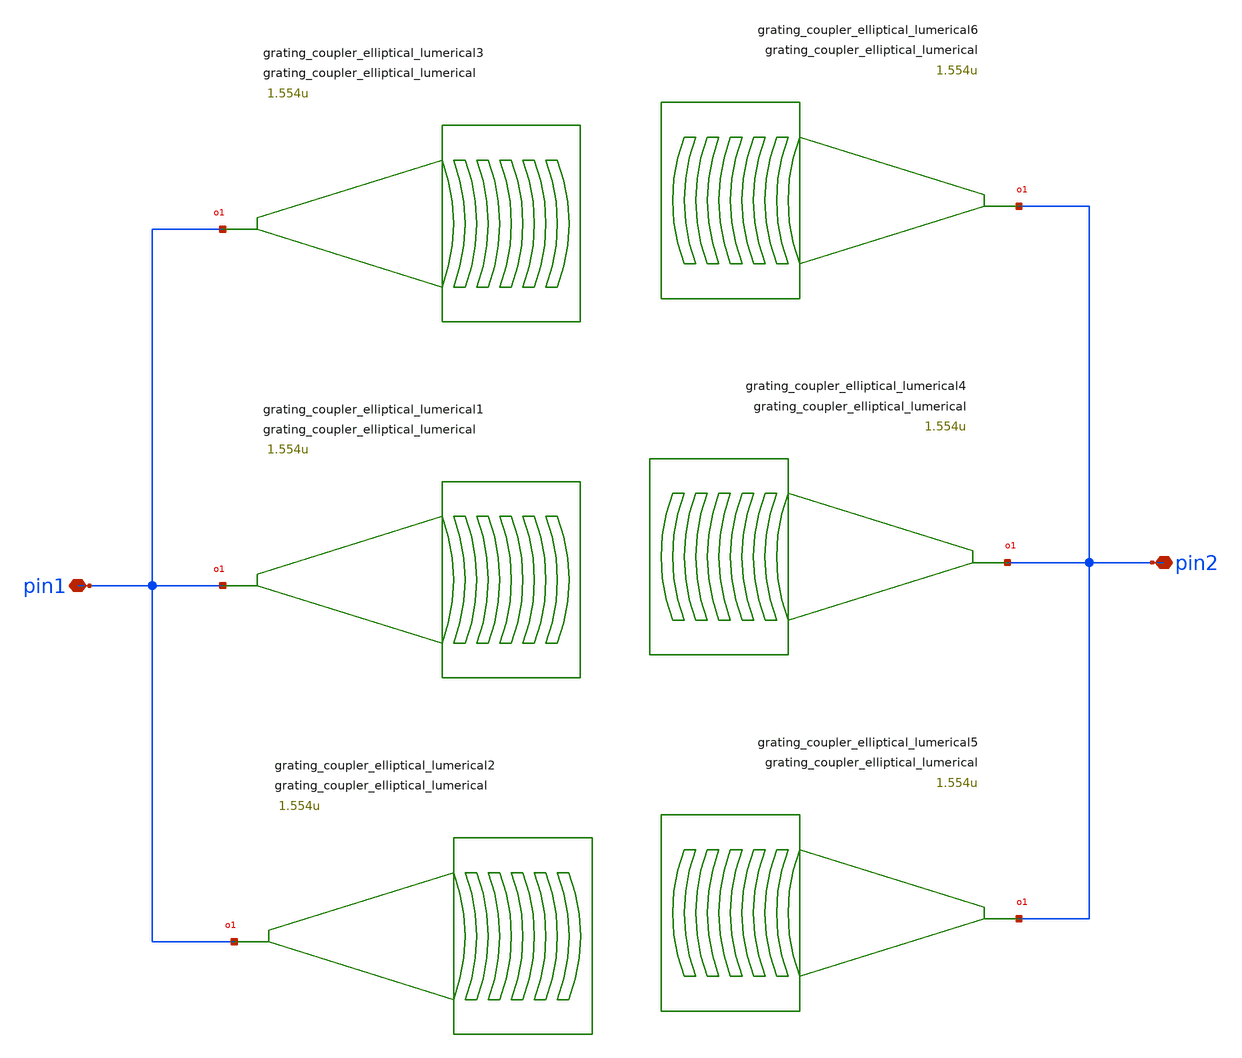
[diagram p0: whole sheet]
** sch_path: xschem/tests/test_sch/test_grating_coupler_elliptical_lumerical.sch
* Copyright (c) 2024, Mabrains LLC
* Licensed under the GNU Lesser General Public License, Version 3.0 (the "License");
* you may not use this file except in compliance with the License.
* GNU Lesser General Public License
* Version 3, 29 June 2007
* This program is free software: you can redistribute it and/or modify
* it under the terms of the GNU Lesser General Public License as published
* by the Free Software Foundation, either version 3 of the License, or
* (at your option) any later version.
* This program is distributed in the hope that it will be useful,
* but WITHOUT ANY WARRANTY; without even the implied warranty of
* MERCHANTABILITY or FITNESS FOR A PARTICULAR PURPOSE.  See the
* GNU Lesser General Public License for more details.
* You should have received a copy of the GNU Lesser General Public License
* along with this program.  If not, see <https://www.gnu.org/licenses/>.
* SPDX-License-Identifier: LGPL-3.0
**.subckt test_grating_coupler_elliptical_lumerical pin1 pin2
*.iopin pin1
*.iopin pin2
Pgrating_coupler_elliptical_lumerical1 pin1 grating_coupler_elliptical_lumerical parameters=[-2.43u,
+ 0.1u, 0.48u] taper_angle=55.0 taper_length=12.6u fiber_angle=5.0 bias_gap=0.0u wavelength=1.554u
Pgrating_coupler_elliptical_lumerical2 pin1 grating_coupler_elliptical_lumerical parameters=[-2.43u,
+ 0.1u, 0.48u] taper_angle=55.0 taper_length=12.6u fiber_angle=5.0 bias_gap=0.0u wavelength=1.554u
Pgrating_coupler_elliptical_lumerical3 pin1 grating_coupler_elliptical_lumerical parameters=[-2.43u,
+ 0.1u, 0.48u] taper_angle=55.0 taper_length=12.6u fiber_angle=5.0 bias_gap=0.0u wavelength=1.554u
Pgrating_coupler_elliptical_lumerical4 pin2 grating_coupler_elliptical_lumerical parameters=[-2.43u,
+ 0.1u, 0.48u] taper_angle=55.0 taper_length=12.6u fiber_angle=5.0 bias_gap=0.0u wavelength=1.554u
Pgrating_coupler_elliptical_lumerical5 pin2 grating_coupler_elliptical_lumerical parameters=[-2.43u,
+ 0.1u, 0.48u] taper_angle=55.0 taper_length=12.6u fiber_angle=5.0 bias_gap=0.0u wavelength=1.554u
Pgrating_coupler_elliptical_lumerical6 pin2 grating_coupler_elliptical_lumerical parameters=[-2.43u,
+ 0.1u, 0.48u] taper_angle=55.0 taper_length=12.6u fiber_angle=5.0 bias_gap=0.0u wavelength=1.554u
**.ends
.end
